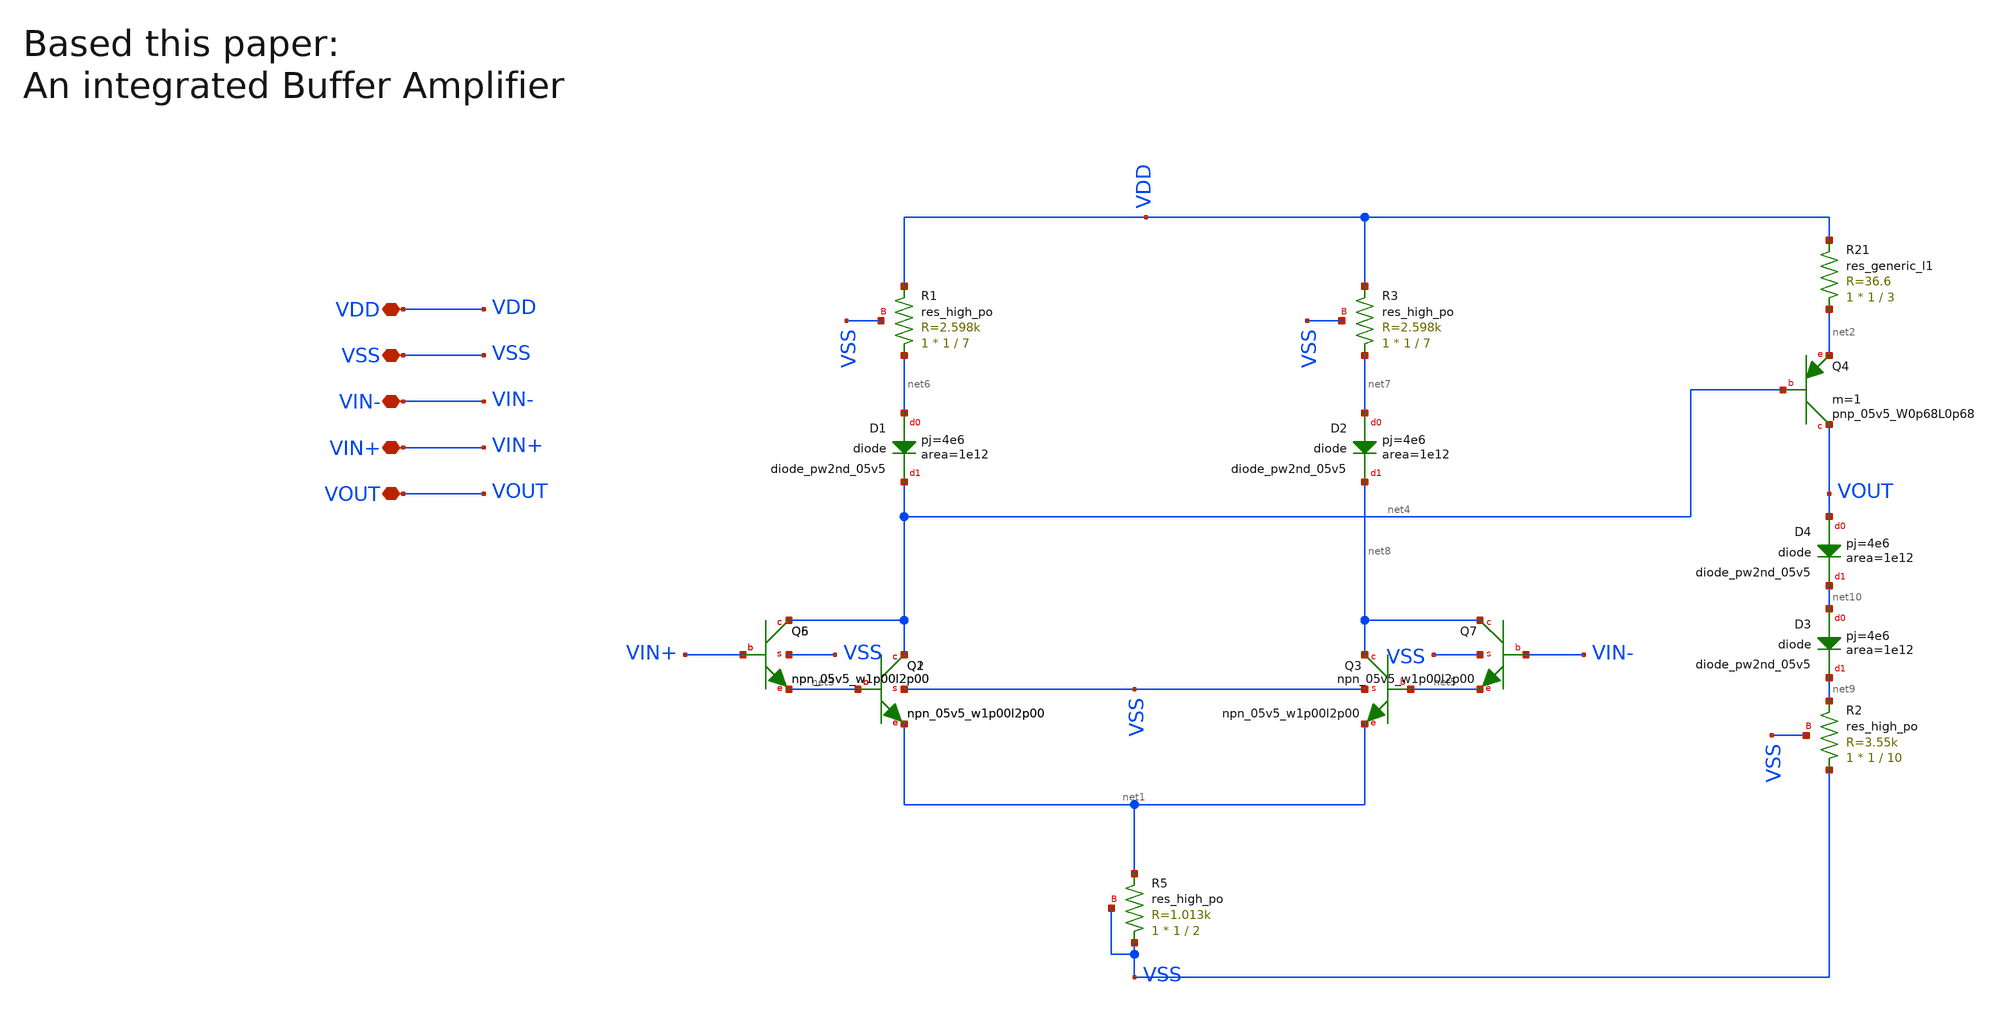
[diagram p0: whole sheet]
** sch_path: my_ip/LIB/Sky130A/single ended amplifiers/BIP002_PMOS_5_sky130A.sch
**.subckt BIP002_PMOS_5_sky130A VDD VSS VIN- VIN+ VOUT
*.iopin VDD
*.iopin VSS
*.iopin VIN-
*.iopin VIN+
*.iopin VOUT
XQ2 net4 net3 net1 VSS sky130_fd_pr__npn_05v5_w1p00l2p00
XQ1 net4 net3 net1 VSS sky130_fd_pr__npn_05v5_w1p00l2p00
XQ3 net8 net5 net1 VSS sky130_fd_pr__npn_05v5_w1p00l2p00
XR5 VSS net1 VSS sky130_fd_pr__res_high_po W=1 L=2 mult=1 m=1
XR1 net6 VDD VSS sky130_fd_pr__res_high_po W=1 L=7 mult=1 m=1
XQ4 VOUT net4 net2 sky130_fd_pr__pnp_05v5_W0p68L0p68 m=1
R21 net2 VDD sky130_fd_pr__res_generic_l1 W=1 L=3 m=1
XR2 VSS net9 VSS sky130_fd_pr__res_high_po W=1 L=10 mult=1 m=1
XQ5 net4 VIN+ net3 VSS sky130_fd_pr__npn_05v5_w1p00l2p00
XQ6 net4 VIN+ net3 VSS sky130_fd_pr__npn_05v5_w1p00l2p00
XQ7 net8 VIN- net5 VSS sky130_fd_pr__npn_05v5_w1p00l2p00
XD1 net6 net4 sky130_fd_pr__diode_pw2nd_05v5 area=1e12 pj=4e6
XR3 net7 VDD VSS sky130_fd_pr__res_high_po W=1 L=7 mult=1 m=1
XD2 net7 net8 sky130_fd_pr__diode_pw2nd_05v5 area=1e12 pj=4e6
XD3 net10 net9 sky130_fd_pr__diode_pw2nd_05v5 area=1e12 pj=4e6
XD4 VOUT net10 sky130_fd_pr__diode_pw2nd_05v5 area=1e12 pj=4e6
**.ends
.end
